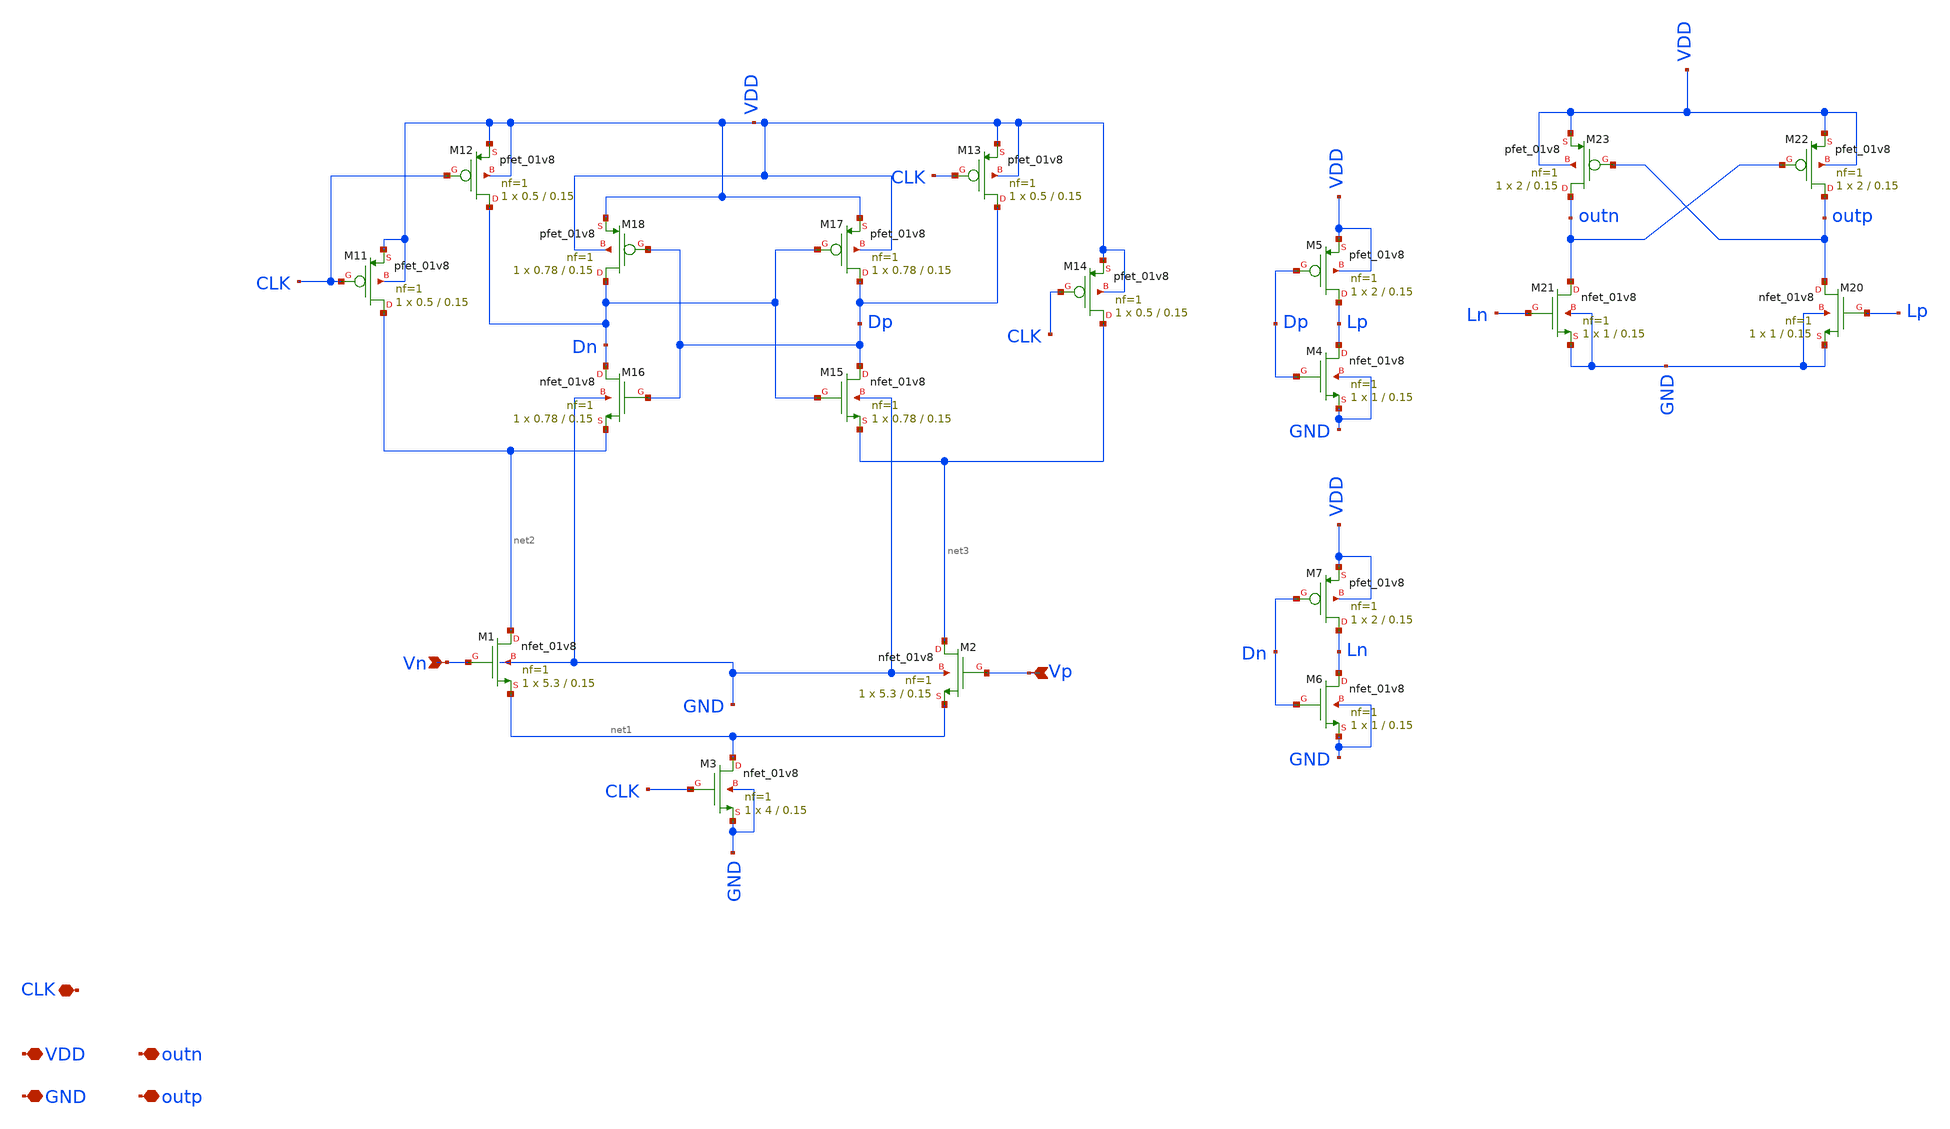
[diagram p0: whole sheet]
** sch_path: xschem/comparator_lvs.sch
**.subckt comparator_lvs VDD GND Vp Vn CLK outn outp
*.iopin VDD
*.iopin GND
*.ipin Vp
*.ipin Vn
*.iopin CLK
*.iopin outn
*.iopin outp
XM1 net2 Vn net1 GND sky130_fd_pr__nfet_01v8 L=0.15 W=5.3 nf=1 ad='int((nf+1)/2) * W/nf * 0.29' as='int((nf+2)/2) * W/nf * 0.29'
+ pd='2*int((nf+1)/2) * (W/nf + 0.29)' ps='2*int((nf+2)/2) * (W/nf + 0.29)' nrd='0.29 / W' nrs='0.29 / W'
+ sa=0 sb=0 sd=0 mult=1 m=1
XM2 net3 Vp net1 GND sky130_fd_pr__nfet_01v8 L=0.15 W=5.3 nf=1 ad='int((nf+1)/2) * W/nf * 0.29' as='int((nf+2)/2) * W/nf * 0.29'
+ pd='2*int((nf+1)/2) * (W/nf + 0.29)' ps='2*int((nf+2)/2) * (W/nf + 0.29)' nrd='0.29 / W' nrs='0.29 / W'
+ sa=0 sb=0 sd=0 mult=1 m=1
XM3 net1 CLK GND GND sky130_fd_pr__nfet_01v8 L=0.15 W=4 nf=1 ad='int((nf+1)/2) * W/nf * 0.29' as='int((nf+2)/2) * W/nf * 0.29'
+ pd='2*int((nf+1)/2) * (W/nf + 0.29)' ps='2*int((nf+2)/2) * (W/nf + 0.29)' nrd='0.29 / W' nrs='0.29 / W'
+ sa=0 sb=0 sd=0 mult=1 m=1
XM11 net2 CLK VDD VDD sky130_fd_pr__pfet_01v8 L=0.15 W=0.5 nf=1 ad='int((nf+1)/2) * W/nf * 0.29' as='int((nf+2)/2) * W/nf * 0.29'
+ pd='2*int((nf+1)/2) * (W/nf + 0.29)' ps='2*int((nf+2)/2) * (W/nf + 0.29)' nrd='0.29 / W' nrs='0.29 / W'
+ sa=0 sb=0 sd=0 mult=1 m=1
XM12 Dn CLK VDD VDD sky130_fd_pr__pfet_01v8 L=0.15 W=0.5 nf=1 ad='int((nf+1)/2) * W/nf * 0.29' as='int((nf+2)/2) * W/nf * 0.29'
+ pd='2*int((nf+1)/2) * (W/nf + 0.29)' ps='2*int((nf+2)/2) * (W/nf + 0.29)' nrd='0.29 / W' nrs='0.29 / W'
+ sa=0 sb=0 sd=0 mult=1 m=1
XM13 Dp CLK VDD VDD sky130_fd_pr__pfet_01v8 L=0.15 W=0.5 nf=1 ad='int((nf+1)/2) * W/nf * 0.29' as='int((nf+2)/2) * W/nf * 0.29'
+ pd='2*int((nf+1)/2) * (W/nf + 0.29)' ps='2*int((nf+2)/2) * (W/nf + 0.29)' nrd='0.29 / W' nrs='0.29 / W'
+ sa=0 sb=0 sd=0 mult=1 m=1
XM14 net3 CLK VDD VDD sky130_fd_pr__pfet_01v8 L=0.15 W=0.5 nf=1 ad='int((nf+1)/2) * W/nf * 0.29' as='int((nf+2)/2) * W/nf * 0.29'
+ pd='2*int((nf+1)/2) * (W/nf + 0.29)' ps='2*int((nf+2)/2) * (W/nf + 0.29)' nrd='0.29 / W' nrs='0.29 / W'
+ sa=0 sb=0 sd=0 mult=1 m=1
XM15 Dp Dn net3 GND sky130_fd_pr__nfet_01v8 L=0.15 W=0.78 nf=1 ad='int((nf+1)/2) * W/nf * 0.29' as='int((nf+2)/2) * W/nf * 0.29'
+ pd='2*int((nf+1)/2) * (W/nf + 0.29)' ps='2*int((nf+2)/2) * (W/nf + 0.29)' nrd='0.29 / W' nrs='0.29 / W'
+ sa=0 sb=0 sd=0 mult=1 m=1
XM16 Dn Dp net2 GND sky130_fd_pr__nfet_01v8 L=0.15 W=0.78 nf=1 ad='int((nf+1)/2) * W/nf * 0.29' as='int((nf+2)/2) * W/nf * 0.29'
+ pd='2*int((nf+1)/2) * (W/nf + 0.29)' ps='2*int((nf+2)/2) * (W/nf + 0.29)' nrd='0.29 / W' nrs='0.29 / W'
+ sa=0 sb=0 sd=0 mult=1 m=1
XM17 Dp Dn VDD VDD sky130_fd_pr__pfet_01v8 L=0.15 W=0.78 nf=1 ad='int((nf+1)/2) * W/nf * 0.29' as='int((nf+2)/2) * W/nf * 0.29'
+ pd='2*int((nf+1)/2) * (W/nf + 0.29)' ps='2*int((nf+2)/2) * (W/nf + 0.29)' nrd='0.29 / W' nrs='0.29 / W'
+ sa=0 sb=0 sd=0 mult=1 m=1
XM18 Dn Dp VDD VDD sky130_fd_pr__pfet_01v8 L=0.15 W=0.78 nf=1 ad='int((nf+1)/2) * W/nf * 0.29' as='int((nf+2)/2) * W/nf * 0.29'
+ pd='2*int((nf+1)/2) * (W/nf + 0.29)' ps='2*int((nf+2)/2) * (W/nf + 0.29)' nrd='0.29 / W' nrs='0.29 / W'
+ sa=0 sb=0 sd=0 mult=1 m=1
XM20 outp Lp GND GND sky130_fd_pr__nfet_01v8 L=0.15 W=1 nf=1 ad='int((nf+1)/2) * W/nf * 0.29' as='int((nf+2)/2) * W/nf * 0.29'
+ pd='2*int((nf+1)/2) * (W/nf + 0.29)' ps='2*int((nf+2)/2) * (W/nf + 0.29)' nrd='0.29 / W' nrs='0.29 / W'
+ sa=0 sb=0 sd=0 mult=1 m=1
XM21 outn Ln GND GND sky130_fd_pr__nfet_01v8 L=0.15 W=1 nf=1 ad='int((nf+1)/2) * W/nf * 0.29' as='int((nf+2)/2) * W/nf * 0.29'
+ pd='2*int((nf+1)/2) * (W/nf + 0.29)' ps='2*int((nf+2)/2) * (W/nf + 0.29)' nrd='0.29 / W' nrs='0.29 / W'
+ sa=0 sb=0 sd=0 mult=1 m=1
XM22 outp outn VDD VDD sky130_fd_pr__pfet_01v8 L=0.15 W=2 nf=1 ad='int((nf+1)/2) * W/nf * 0.29' as='int((nf+2)/2) * W/nf * 0.29'
+ pd='2*int((nf+1)/2) * (W/nf + 0.29)' ps='2*int((nf+2)/2) * (W/nf + 0.29)' nrd='0.29 / W' nrs='0.29 / W'
+ sa=0 sb=0 sd=0 mult=1 m=1
XM23 outn outp VDD VDD sky130_fd_pr__pfet_01v8 L=0.15 W=2 nf=1 ad='int((nf+1)/2) * W/nf * 0.29' as='int((nf+2)/2) * W/nf * 0.29'
+ pd='2*int((nf+1)/2) * (W/nf + 0.29)' ps='2*int((nf+2)/2) * (W/nf + 0.29)' nrd='0.29 / W' nrs='0.29 / W'
+ sa=0 sb=0 sd=0 mult=1 m=1
XM4 Lp Dp GND GND sky130_fd_pr__nfet_01v8 L=0.15 W=1 nf=1 ad='int((nf+1)/2) * W/nf * 0.29' as='int((nf+2)/2) * W/nf * 0.29'
+ pd='2*int((nf+1)/2) * (W/nf + 0.29)' ps='2*int((nf+2)/2) * (W/nf + 0.29)' nrd='0.29 / W' nrs='0.29 / W'
+ sa=0 sb=0 sd=0 mult=1 m=1
XM5 Lp Dp VDD VDD sky130_fd_pr__pfet_01v8 L=0.15 W=2 nf=1 ad='int((nf+1)/2) * W/nf * 0.29' as='int((nf+2)/2) * W/nf * 0.29'
+ pd='2*int((nf+1)/2) * (W/nf + 0.29)' ps='2*int((nf+2)/2) * (W/nf + 0.29)' nrd='0.29 / W' nrs='0.29 / W'
+ sa=0 sb=0 sd=0 mult=1 m=1
XM6 Ln Dn GND GND sky130_fd_pr__nfet_01v8 L=0.15 W=1 nf=1 ad='int((nf+1)/2) * W/nf * 0.29' as='int((nf+2)/2) * W/nf * 0.29'
+ pd='2*int((nf+1)/2) * (W/nf + 0.29)' ps='2*int((nf+2)/2) * (W/nf + 0.29)' nrd='0.29 / W' nrs='0.29 / W'
+ sa=0 sb=0 sd=0 mult=1 m=1
XM7 Ln Dn VDD VDD sky130_fd_pr__pfet_01v8 L=0.15 W=2 nf=1 ad='int((nf+1)/2) * W/nf * 0.29' as='int((nf+2)/2) * W/nf * 0.29'
+ pd='2*int((nf+1)/2) * (W/nf + 0.29)' ps='2*int((nf+2)/2) * (W/nf + 0.29)' nrd='0.29 / W' nrs='0.29 / W'
+ sa=0 sb=0 sd=0 mult=1 m=1
**.ends
.end
